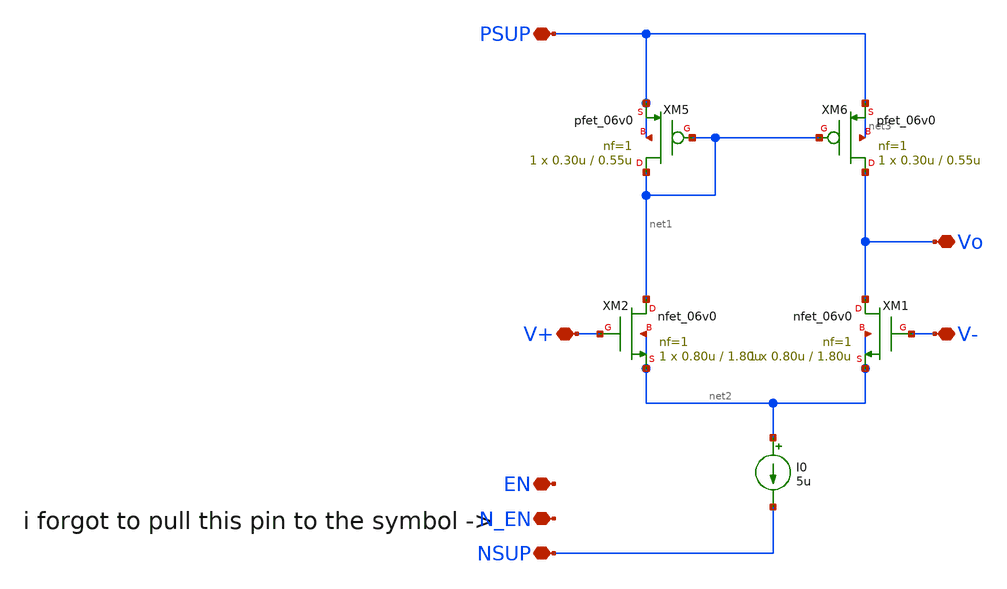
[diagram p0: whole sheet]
** sch_path: Design/lib/aux_amp.sch
**.subckt aux_amp NSUP PSUP V+ V- EN Vo N_EN
*.iopin NSUP
*.iopin PSUP
*.iopin V+
*.iopin V-
*.iopin EN
*.iopin Vo
*.iopin N_EN
XM1 Vo V- net2 net2 nfet_06v0 L=1.80u W=0.80u nf=1 ad='int((nf+1)/2) * W/nf * 0.18u' as='int((nf+2)/2) * W/nf * 0.18u'
+ pd='2*int((nf+1)/2) * (W/nf + 0.18u)' ps='2*int((nf+2)/2) * (W/nf + 0.18u)' nrd='0.18u / W' nrs='0.18u / W'
+ sa=0 sb=0 sd=0 m=1
XM2 net1 V+ net2 net2 nfet_06v0 L=1.80u W=0.80u nf=1 ad='int((nf+1)/2) * W/nf * 0.18u' as='int((nf+2)/2) * W/nf * 0.18u'
+ pd='2*int((nf+1)/2) * (W/nf + 0.18u)' ps='2*int((nf+2)/2) * (W/nf + 0.18u)' nrd='0.18u / W' nrs='0.18u / W'
+ sa=0 sb=0 sd=0 m=1
XM5 net1 net1 PSUP PSUP pfet_06v0 L=0.55u W=0.30u nf=1 ad='int((nf+1)/2) * W/nf * 0.18u' as='int((nf+2)/2) * W/nf * 0.18u'
+ pd='2*int((nf+1)/2) * (W/nf + 0.18u)' ps='2*int((nf+2)/2) * (W/nf + 0.18u)' nrd='0.18u / W' nrs='0.18u / W'
+ sa=0 sb=0 sd=0 m=1
XM6 Vo net1 PSUP net3 pfet_06v0 L=0.55u W=0.30u nf=1 ad='int((nf+1)/2) * W/nf * 0.18u' as='int((nf+2)/2) * W/nf * 0.18u'
+ pd='2*int((nf+1)/2) * (W/nf + 0.18u)' ps='2*int((nf+2)/2) * (W/nf + 0.18u)' nrd='0.18u / W' nrs='0.18u / W'
+ sa=0 sb=0 sd=0 m=1
I0 net2 NSUP 5u
**** begin user architecture code
i forgot to pull this pin to the symbol ->
**** end user architecture code
**.ends
.end
